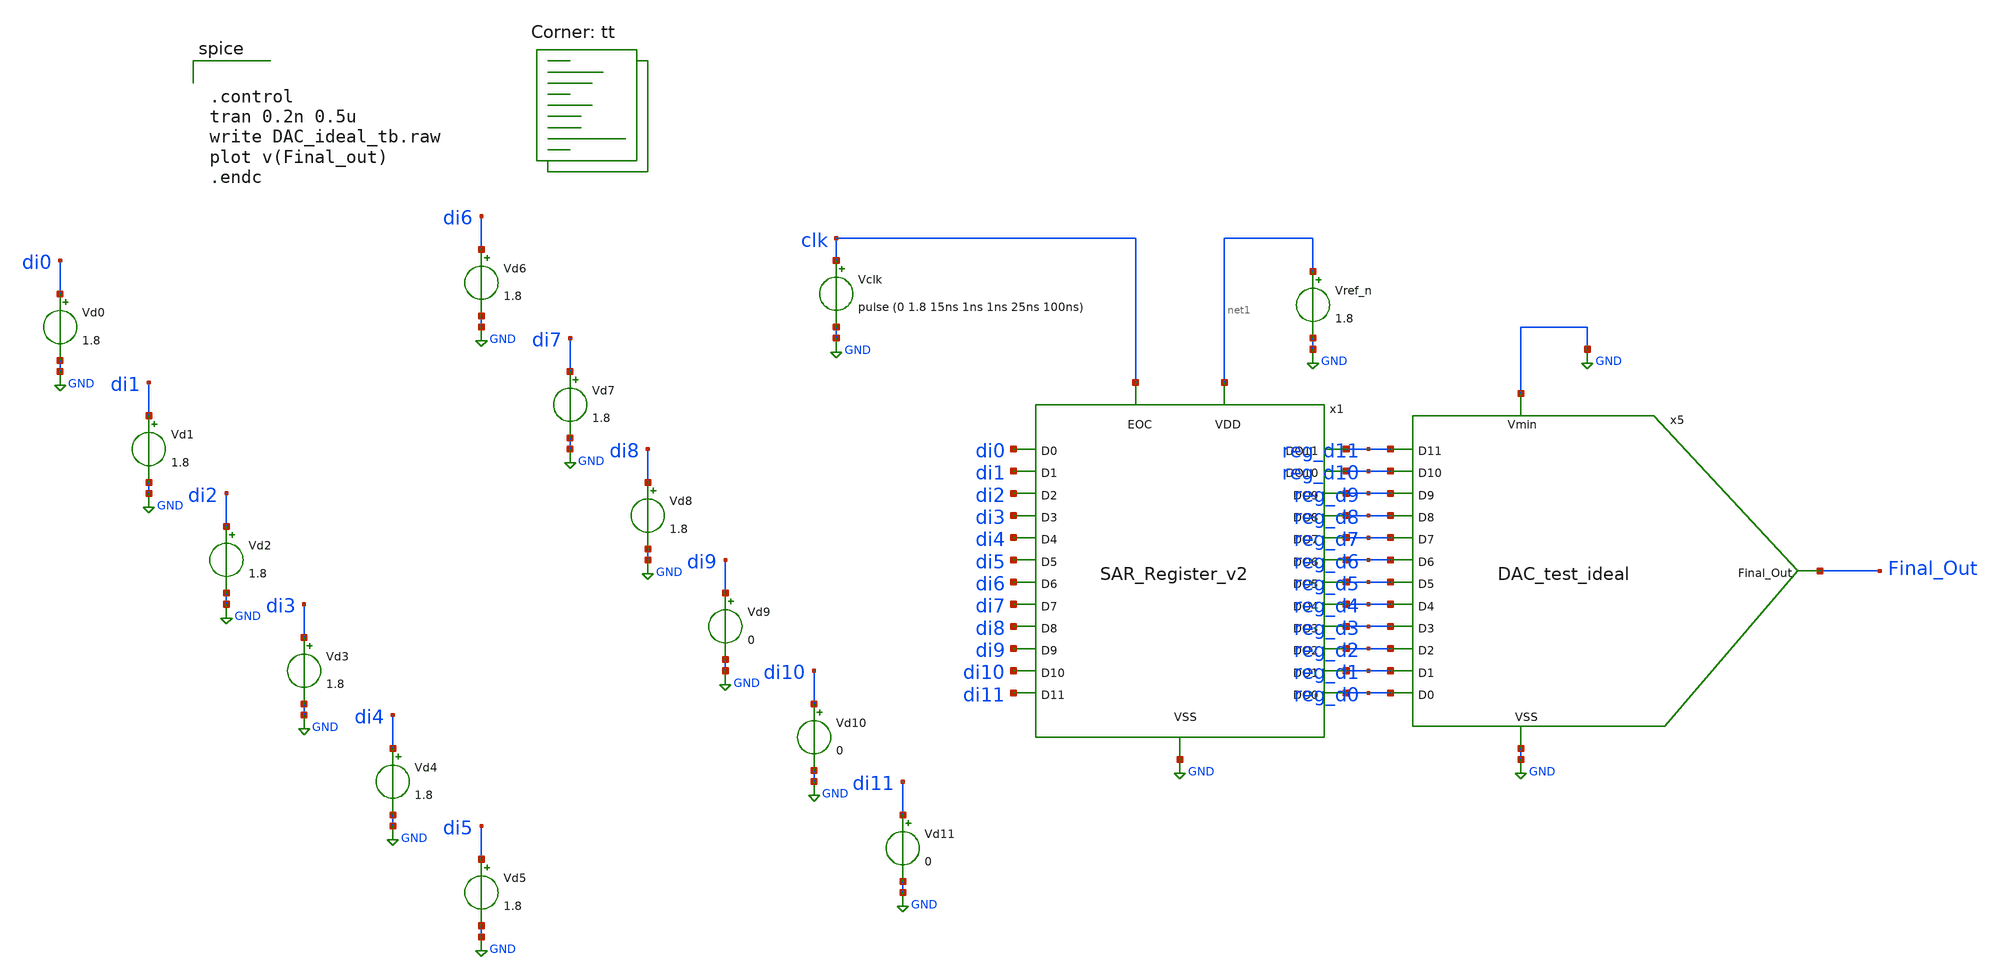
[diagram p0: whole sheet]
** sch_path: DAC_ideal_tb.sch
**.subckt DAC_ideal_tb
Vd0 di0 GND 1.8
Vd1 di1 GND 1.8
Vd2 di2 GND 1.8
Vd3 di3 GND 1.8
Vd4 di4 GND 1.8
Vd5 di5 GND 1.8
Vd6 di6 GND 1.8
Vd7 di7 GND 1.8
Vd8 di8 GND 1.8
Vd9 di9 GND 0
Vd10 di10 GND 0
Vd11 di11 GND 0
Vref_n net1 GND 1.8
Vclk clk GND pulse (0 1.8 15ns 1ns 1ns 25ns 100ns)
x1 net1 di8 di5 di11 di2 reg_d11 reg_d8 reg_d5 reg_d2 clk di7 di1 di10 di4 reg_d1 reg_d4 reg_d7
+ reg_d10 di0 di3 di6 di9 reg_d0 reg_d3 reg_d6 reg_d9 GND SAR_Register_v2
x5 Final_Out GND GND reg_d7 reg_d3 reg_d11 reg_d10 reg_d6 reg_d2 reg_d5 reg_d1 reg_d9 reg_d0 reg_d4
+ reg_d8 DAC_test_ideal
**** begin user architecture code


.control
tran 0.2n 0.5u
write DAC_ideal_tb.raw
plot v(Final_out)
.endc


.lib $::SKYWATER_MODELS/sky130.lib.spice tt
**** end user architecture code
**.ends

* expanding   symbol:  project/SAR_Register_v2.sym # of pins=27
** sym_path: SAR_Register_v2.sym
** sch_path: SAR_Register_v2.sch
.subckt SAR_Register_v2 VDD D8 D5 D11 D2 DO11 DO8 DO5 DO2 EOC D7 D1 D10 D4 DO1 DO4 DO7 DO10 D0 D3 D6
+ D9 DO0 DO3 DO6 DO9 VSS
*.ipin VDD
*.ipin VSS
*.ipin D11
*.ipin D10
*.ipin D9
*.ipin D8
*.ipin D7
*.ipin D6
*.ipin D5
*.ipin D4
*.ipin D3
*.ipin D2
*.ipin D1
*.ipin D0
*.opin DO11
*.opin DO10
*.opin DO9
*.opin DO8
*.opin DO7
*.opin DO6
*.opin DO3
*.opin DO4
*.opin DO5
*.opin DO2
*.opin DO1
*.opin DO0
*.ipin EOC
x1 DO11 D11 VDD EOC VSS FFD_logic
x2 DO10 D10 VDD EOC VSS FFD_logic
x3 DO9 D9 VDD EOC VSS FFD_logic
x4 DO8 D8 VDD EOC VSS FFD_logic
x5 DO7 D7 VDD EOC VSS FFD_logic
x6 DO6 D6 VDD EOC VSS FFD_logic
x7 DO3 D3 VDD EOC VSS FFD_logic
x8 DO4 D4 VDD EOC VSS FFD_logic
x9 DO5 D5 VDD EOC VSS FFD_logic
x10 DO2 D2 VDD EOC VSS FFD_logic
x11 DO1 D1 VDD EOC VSS FFD_logic
x12 DO0 D0 VDD EOC VSS FFD_logic
.ends


* expanding   symbol:  project/DAC_test_ideal.sym # of pins=15
** sym_path: DAC_test_ideal.sym
** sch_path: DAC_test_ideal.sch
.subckt DAC_test_ideal Final_Out VSS Vmin D7 D3 D11 D10 D6 D2 D5 D1 D9 D0 D4 D8
*.ipin D11
*.ipin D10
*.ipin D9
*.ipin D8
*.ipin D7
*.ipin D6
*.ipin D5
*.ipin D4
*.ipin D3
*.ipin D2
*.ipin D1
*.ipin D0
*.ipin Vmin
*.ipin VSS
*.opin Final_Out
E1 net12 net1 D11 VSS 0.5
E2 net1 net2 D10 VSS 0.25
E3 net2 net3 D9 VSS 0.125
E4 net3 net4 D8 VSS 0.0625
E5 net4 net5 D7 VSS 0.03125
E6 net5 net6 D6 VSS 0.015625
E7 net6 net7 D5 VSS 7.8125e-3
E8 net7 net8 D4 VSS 3.90625e-3
E9 net8 net9 D3 VSS 1.953125e-3
E10 net9 net10 D2 VSS 9.765625e-4
E11 net10 net11 D1 VSS 4.8828125e-4
E12 net11 VSS D0 VSS 2.44140625e-4
E13 Final_Out Vmin net12 VSS {gain}
.ends


* expanding   symbol:  FFD_logic.sym # of pins=5
** sym_path: FFD_logic.sym
** sch_path: FFD_logic.sch
.subckt FFD_logic Q D VDD CLK VSS
*.ipin D
*.ipin CLK
*.ipin VDD
*.ipin VSS
*.opin Q
x1 VDD net3 D net2 VSS nand_FFD
x2 VDD net4 net2 net1 VSS nand_FFD
x3 VDD net5 net3 net6 VSS nand_FFD
x4 VDD net6 net5 net4 VSS nand_FFD
x5 VDD net8 net5 CLK VSS nand_FFD
x6 VDD net7 CLK net6 VSS nand_FFD
x7 VDD Q net8 net9 VSS nand_FFD
x8 VDD net9 Q net7 VSS nand_FFD
x9 VDD D net1 VSS Inverter
x10 VDD CLK net2 VSS Inverter
.ends


* expanding   symbol:  nand_FFD.sym # of pins=5
** sym_path: nand_FFD.sym
** sch_path: nand_FFD.sch
.subckt nand_FFD VDD Y A B VSS
*.ipin VDD
*.ipin A
*.ipin B
*.ipin VSS
*.opin Y
XM1 Y A net1 VSS sky130_fd_pr__nfet_01v8 L=0.15 W=1 nf=1 ad='int((nf+1)/2) * W/nf * 0.29' as='int((nf+2)/2) * W/nf * 0.29'
+ pd='2*int((nf+1)/2) * (W/nf + 0.29)' ps='2*int((nf+2)/2) * (W/nf + 0.29)' nrd='0.29 / W' nrs='0.29 / W'
+ sa=0 sb=0 sd=0 mult=1 m=1
XM2 net1 B VSS VSS sky130_fd_pr__nfet_01v8 L=0.15 W=1 nf=1 ad='int((nf+1)/2) * W/nf * 0.29' as='int((nf+2)/2) * W/nf * 0.29'
+ pd='2*int((nf+1)/2) * (W/nf + 0.29)' ps='2*int((nf+2)/2) * (W/nf + 0.29)' nrd='0.29 / W' nrs='0.29 / W'
+ sa=0 sb=0 sd=0 mult=1 m=1
XM3 Y A VDD VDD sky130_fd_pr__pfet_01v8 L=0.15 W=2 nf=1 ad='int((nf+1)/2) * W/nf * 0.29' as='int((nf+2)/2) * W/nf * 0.29'
+ pd='2*int((nf+1)/2) * (W/nf + 0.29)' ps='2*int((nf+2)/2) * (W/nf + 0.29)' nrd='0.29 / W' nrs='0.29 / W'
+ sa=0 sb=0 sd=0 mult=1 m=1
XM4 Y B VDD VDD sky130_fd_pr__pfet_01v8 L=0.15 W=2 nf=1 ad='int((nf+1)/2) * W/nf * 0.29' as='int((nf+2)/2) * W/nf * 0.29'
+ pd='2*int((nf+1)/2) * (W/nf + 0.29)' ps='2*int((nf+2)/2) * (W/nf + 0.29)' nrd='0.29 / W' nrs='0.29 / W'
+ sa=0 sb=0 sd=0 mult=1 m=1
.ends


* expanding   symbol:  Inverter.sym # of pins=4
** sym_path: Inverter.sym
** sch_path: Inverter.sch
.subckt Inverter VDD IN OUT VSS
*.ipin IN
*.ipin VSS
*.ipin VDD
*.opin OUT
XM1 OUT IN VSS VSS sky130_fd_pr__nfet_01v8 L=0.3 W=1 nf=1 ad='int((nf+1)/2) * W/nf * 0.29' as='int((nf+2)/2) * W/nf * 0.29'
+ pd='2*int((nf+1)/2) * (W/nf + 0.29)' ps='2*int((nf+2)/2) * (W/nf + 0.29)' nrd='0.29 / W' nrs='0.29 / W'
+ sa=0 sb=0 sd=0 mult=1 m=1
XM2 OUT IN VDD VDD sky130_fd_pr__pfet_01v8 L=0.3 W=2 nf=1 ad='int((nf+1)/2) * W/nf * 0.29' as='int((nf+2)/2) * W/nf * 0.29'
+ pd='2*int((nf+1)/2) * (W/nf + 0.29)' ps='2*int((nf+2)/2) * (W/nf + 0.29)' nrd='0.29 / W' nrs='0.29 / W'
+ sa=0 sb=0 sd=0 mult=1 m=1
.ends

.GLOBAL GND
.end
